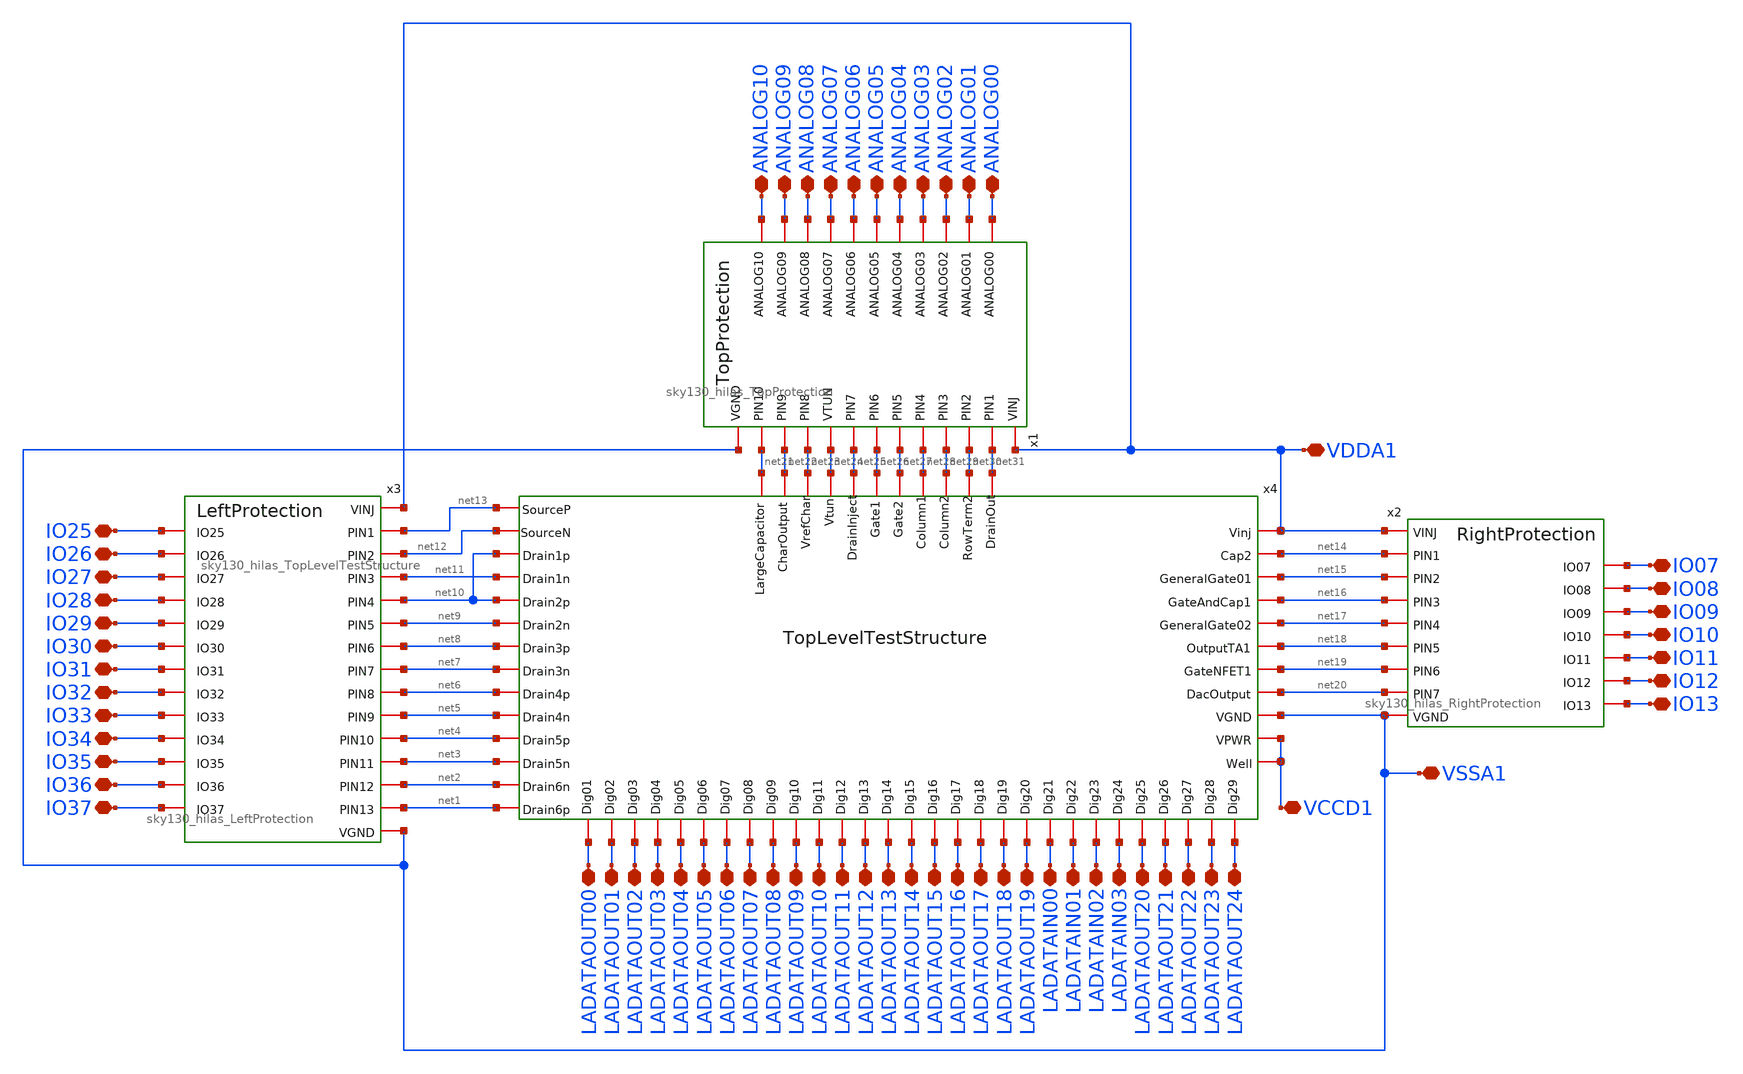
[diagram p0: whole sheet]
** sch_path: libs.ref/sky130_hilas_sc/xschem/sky130_hilas_TopLevelProtectionPins.sch
**.subckt sky130_hilas_TopLevelProtectionPins IO07 IO25 ANALOG00 ANALOG01 ANALOG02 ANALOG03 ANALOG04
*+ ANALOG05 ANALOG06 ANALOG07 ANALOG08 ANALOG09 ANALOG10 IO26 IO27 LADATAIN00 VSSA1 IO08 IO09 IO10 IO11 IO12
*+ IO13 IO28 IO29 IO30 IO31 IO32 IO33 IO34 IO35 IO36 IO37 VDDA1 LADATAOUT01 VCCD1 LADATAOUT00 LADATAOUT03
*+ LADATAOUT02 LADATAOUT05 LADATAOUT04 LADATAOUT07 LADATAOUT06 LADATAOUT09 LADATAOUT08 LADATAOUT11 LADATAOUT10
*+ LADATAOUT13 LADATAOUT12 LADATAOUT14 LADATAOUT15 LADATAOUT16 LADATAOUT17 LADATAOUT18 LADATAOUT19 LADATAOUT20
*+ LADATAOUT21 LADATAOUT22 LADATAOUT23 LADATAOUT24 LADATAIN01 LADATAIN02 LADATAIN03
*.iopin IO07
*.iopin IO25
*.iopin ANALOG00
*.iopin ANALOG01
*.iopin ANALOG02
*.iopin ANALOG03
*.iopin ANALOG04
*.iopin ANALOG05
*.iopin ANALOG06
*.iopin ANALOG07
*.iopin ANALOG08
*.iopin ANALOG09
*.iopin ANALOG10
*.iopin IO26
*.iopin IO27
*.iopin LADATAIN00
*.iopin VSSA1
*.iopin IO08
*.iopin IO09
*.iopin IO10
*.iopin IO11
*.iopin IO12
*.iopin IO13
*.iopin IO28
*.iopin IO29
*.iopin IO30
*.iopin IO31
*.iopin IO32
*.iopin IO33
*.iopin IO34
*.iopin IO35
*.iopin IO36
*.iopin IO37
*.iopin VDDA1
*.iopin LADATAOUT01
*.iopin VCCD1
*.iopin LADATAOUT00
*.iopin LADATAOUT03
*.iopin LADATAOUT02
*.iopin LADATAOUT05
*.iopin LADATAOUT04
*.iopin LADATAOUT07
*.iopin LADATAOUT06
*.iopin LADATAOUT09
*.iopin LADATAOUT08
*.iopin LADATAOUT11
*.iopin LADATAOUT10
*.iopin LADATAOUT13
*.iopin LADATAOUT12
*.iopin LADATAOUT14
*.iopin LADATAOUT15
*.iopin LADATAOUT16
*.iopin LADATAOUT17
*.iopin LADATAOUT18
*.iopin LADATAOUT19
*.iopin LADATAOUT20
*.iopin LADATAOUT21
*.iopin LADATAOUT22
*.iopin LADATAOUT23
*.iopin LADATAOUT24
*.iopin LADATAIN01
*.iopin LADATAIN02
*.iopin LADATAIN03
x1 VDDA1 ANALOG00 net31 ANALOG01 net30 ANALOG02 net29 ANALOG03 net28 ANALOG04 net27 ANALOG05 net26
+ ANALOG06 net25 net24 ANALOG07 ANALOG08 net23 ANALOG09 net22 ANALOG10 net21 VSSA1 sky130_hilas_TopProtection
x2 VDDA1 IO07 net14 IO08 net15 IO09 net16 IO10 net17 IO11 net18 IO12 net19 IO13 net20 VSSA1
+ sky130_hilas_RightProtection
x3 VDDA1 IO25 net13 IO26 net12 IO27 net11 IO28 net10 IO29 net9 IO30 net8 IO31 net7 IO32 net6 IO33
+ net5 IO34 net4 IO35 net3 IO36 net2 IO37 net1 VSSA1 sky130_hilas_LeftProtection
x4 LADATAOUT00 LADATAOUT24 LADATAOUT23 LADATAOUT22 LADATAOUT20 LADATAOUT21 LADATAOUT17 LADATAOUT19
+ LADATAOUT18 LADATAOUT15 LADATAOUT16 LADATAOUT02 LADATAOUT03 LADATAOUT04 net31 LADATAOUT05 LADATAOUT06
+ LADATAOUT07 LADATAOUT08 LADATAOUT12 LADATAOUT01 net18 VCCD1 net13 net12 net10 net11 net10 net9 net8 net7 net6
+ net21 net5 net29 net4 net28 net3 net2 LADATAIN00 LADATAIN01 LADATAIN02 LADATAIN03 VSSA1 net1 net27 net26
+ net25 VCCD1 net23 net30 net22 net14 net15 net16 LADATAOUT09 net17 LADATAOUT13 net20 LADATAOUT14 net24
+ LADATAOUT11 VDDA1 LADATAOUT10 net19 sky130_hilas_TopLevelTestStructure
**.ends
.end
